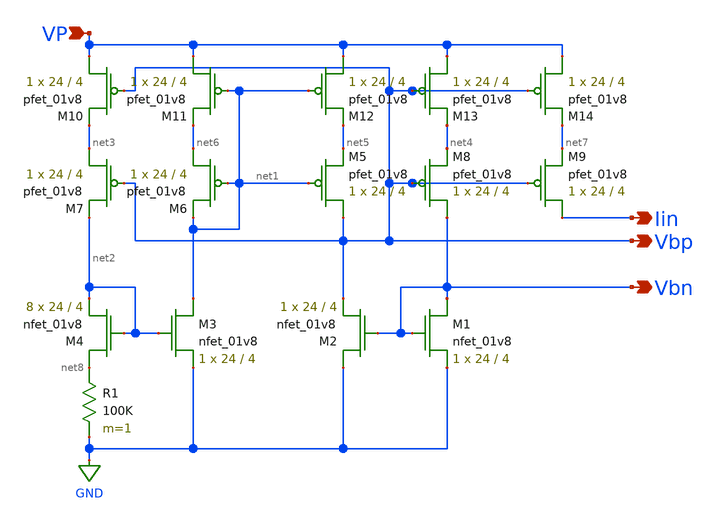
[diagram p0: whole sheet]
** sch_path: xschem/biasGen.sch
**.subckt biasGen Iin VP Vbp Vbn
*.opin Iin
*.ipin VP
*.opin Vbp
*.opin Vbn
XM1 Vbn Vbn GND GND sky130_fd_pr__nfet_01v8 L=4 W=24 nf=1 ad='int((nf+1)/2) * W/nf * 0.29' as='int((nf+2)/2) * W/nf * 0.29'
+ pd='2*int((nf+1)/2) * (W/nf + 0.29)' ps='2*int((nf+2)/2) * (W/nf + 0.29)' nrd='0.29 / W' nrs='0.29 / W'
+ sa=0 sb=0 sd=0 mult=1 m=1
XM2 GND Vbn Vbp GND sky130_fd_pr__nfet_01v8 L=4 W=24 nf=1 ad='int((nf+1)/2) * W/nf * 0.29' as='int((nf+2)/2) * W/nf * 0.29'
+ pd='2*int((nf+1)/2) * (W/nf + 0.29)' ps='2*int((nf+2)/2) * (W/nf + 0.29)' nrd='0.29 / W' nrs='0.29 / W'
+ sa=0 sb=0 sd=0 mult=1 m=1
XM3 net1 net2 GND GND sky130_fd_pr__nfet_01v8 L=4 W=24 nf=1 ad='int((nf+1)/2) * W/nf * 0.29' as='int((nf+2)/2) * W/nf * 0.29'
+ pd='2*int((nf+1)/2) * (W/nf + 0.29)' ps='2*int((nf+2)/2) * (W/nf + 0.29)' nrd='0.29 / W' nrs='0.29 / W'
+ sa=0 sb=0 sd=0 mult=1 m=1
XM4 net8 net2 net2 GND sky130_fd_pr__nfet_01v8 L=4 W=24 nf=1 ad='int((nf+1)/2) * W/nf * 0.29' as='int((nf+2)/2) * W/nf * 0.29'
+ pd='2*int((nf+1)/2) * (W/nf + 0.29)' ps='2*int((nf+2)/2) * (W/nf + 0.29)' nrd='0.29 / W' nrs='0.29 / W'
+ sa=0 sb=0 sd=0 mult=8 m=8
XM5 Vbp net1 net5 VDD sky130_fd_pr__pfet_01v8 L=4 W=24 nf=1 ad='int((nf+1)/2) * W/nf * 0.29' as='int((nf+2)/2) * W/nf * 0.29'
+ pd='2*int((nf+1)/2) * (W/nf + 0.29)' ps='2*int((nf+2)/2) * (W/nf + 0.29)' nrd='0.29 / W' nrs='0.29 / W'
+ sa=0 sb=0 sd=0 mult=1 m=1
XM6 net6 net1 net1 VDD sky130_fd_pr__pfet_01v8 L=4 W=24 nf=1 ad='int((nf+1)/2) * W/nf * 0.29' as='int((nf+2)/2) * W/nf * 0.29'
+ pd='2*int((nf+1)/2) * (W/nf + 0.29)' ps='2*int((nf+2)/2) * (W/nf + 0.29)' nrd='0.29 / W' nrs='0.29 / W'
+ sa=0 sb=0 sd=0 mult=1 m=1
XM7 net3 Vbp net2 VDD sky130_fd_pr__pfet_01v8 L=4 W=24 nf=1 ad='int((nf+1)/2) * W/nf * 0.29' as='int((nf+2)/2) * W/nf * 0.29'
+ pd='2*int((nf+1)/2) * (W/nf + 0.29)' ps='2*int((nf+2)/2) * (W/nf + 0.29)' nrd='0.29 / W' nrs='0.29 / W'
+ sa=0 sb=0 sd=0 mult=1 m=1
XM8 Vbn Vbp net4 VDD sky130_fd_pr__pfet_01v8 L=4 W=24 nf=1 ad='int((nf+1)/2) * W/nf * 0.29' as='int((nf+2)/2) * W/nf * 0.29'
+ pd='2*int((nf+1)/2) * (W/nf + 0.29)' ps='2*int((nf+2)/2) * (W/nf + 0.29)' nrd='0.29 / W' nrs='0.29 / W'
+ sa=0 sb=0 sd=0 mult=1 m=1
R1 net8 GND 100K m=1
XM9 Iin Vbp net7 VDD sky130_fd_pr__pfet_01v8 L=4 W=24 nf=1 ad='int((nf+1)/2) * W/nf * 0.29' as='int((nf+2)/2) * W/nf * 0.29'
+ pd='2*int((nf+1)/2) * (W/nf + 0.29)' ps='2*int((nf+2)/2) * (W/nf + 0.29)' nrd='0.29 / W' nrs='0.29 / W'
+ sa=0 sb=0 sd=0 mult=1 m=1
XM10 VP Vbp net3 VDD sky130_fd_pr__pfet_01v8 L=4 W=24 nf=1 ad='int((nf+1)/2) * W/nf * 0.29' as='int((nf+2)/2) * W/nf * 0.29'
+ pd='2*int((nf+1)/2) * (W/nf + 0.29)' ps='2*int((nf+2)/2) * (W/nf + 0.29)' nrd='0.29 / W' nrs='0.29 / W'
+ sa=0 sb=0 sd=0 mult=1 m=1
XM11 VP net1 net6 VDD sky130_fd_pr__pfet_01v8 L=4 W=24 nf=1 ad='int((nf+1)/2) * W/nf * 0.29' as='int((nf+2)/2) * W/nf * 0.29'
+ pd='2*int((nf+1)/2) * (W/nf + 0.29)' ps='2*int((nf+2)/2) * (W/nf + 0.29)' nrd='0.29 / W' nrs='0.29 / W'
+ sa=0 sb=0 sd=0 mult=1 m=1
XM12 VP net1 net5 VDD sky130_fd_pr__pfet_01v8 L=4 W=24 nf=1 ad='int((nf+1)/2) * W/nf * 0.29' as='int((nf+2)/2) * W/nf * 0.29'
+ pd='2*int((nf+1)/2) * (W/nf + 0.29)' ps='2*int((nf+2)/2) * (W/nf + 0.29)' nrd='0.29 / W' nrs='0.29 / W'
+ sa=0 sb=0 sd=0 mult=1 m=1
XM13 VP Vbp net4 VDD sky130_fd_pr__pfet_01v8 L=4 W=24 nf=1 ad='int((nf+1)/2) * W/nf * 0.29' as='int((nf+2)/2) * W/nf * 0.29'
+ pd='2*int((nf+1)/2) * (W/nf + 0.29)' ps='2*int((nf+2)/2) * (W/nf + 0.29)' nrd='0.29 / W' nrs='0.29 / W'
+ sa=0 sb=0 sd=0 mult=1 m=1
XM14 VP Vbp net7 VDD sky130_fd_pr__pfet_01v8 L=4 W=24 nf=1 ad='int((nf+1)/2) * W/nf * 0.29' as='int((nf+2)/2) * W/nf * 0.29'
+ pd='2*int((nf+1)/2) * (W/nf + 0.29)' ps='2*int((nf+2)/2) * (W/nf + 0.29)' nrd='0.29 / W' nrs='0.29 / W'
+ sa=0 sb=0 sd=0 mult=1 m=1
**.ends
.GLOBAL GND
.end
